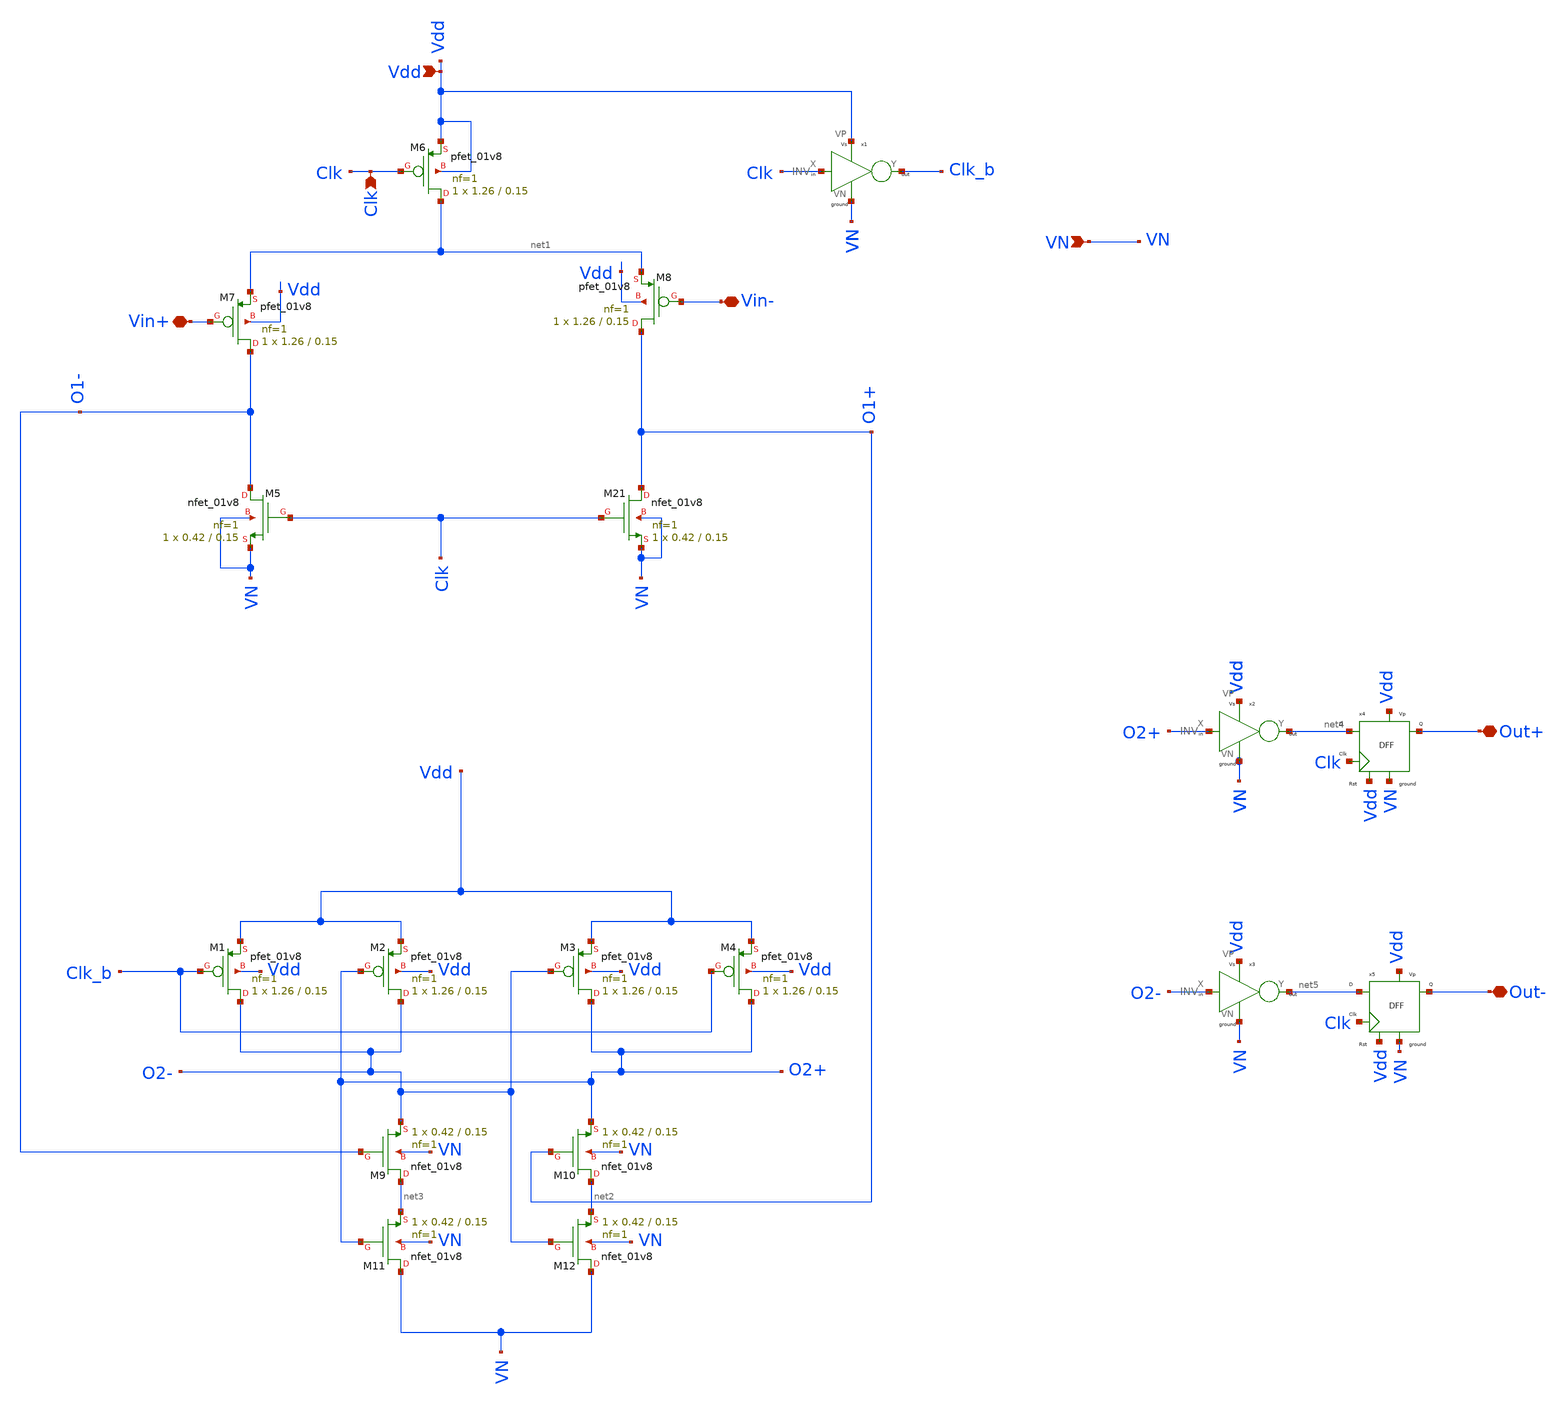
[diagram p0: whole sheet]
** sch_path: Blocks/Conv_comparator/Conv_comp.sch
**.subckt Conv_comp Vin+ Vin- Out+ Out- VN Vdd Clk
*.iopin Vin+
*.iopin Vin-
*.iopin Out+
*.iopin Out-
*.ipin VN
*.ipin Vdd
*.ipin Clk
XM6 net1 Clk Vdd Vdd sky130_fd_pr__pfet_01v8 L=0.15 W=1.26 nf=1 ad='int((nf+1)/2) * W/nf * 0.29' as='int((nf+2)/2) * W/nf * 0.29'
+ pd='2*int((nf+1)/2) * (W/nf + 0.29)' ps='2*int((nf+2)/2) * (W/nf + 0.29)' nrd='0.29 / W' nrs='0.29 / W'
+ sa=0 sb=0 sd=0 mult=1 m=1
XM7 O1- Vin+ net1 Vdd sky130_fd_pr__pfet_01v8 L=0.15 W=1.26 nf=1 ad='int((nf+1)/2) * W/nf * 0.29' as='int((nf+2)/2) * W/nf * 0.29'
+ pd='2*int((nf+1)/2) * (W/nf + 0.29)' ps='2*int((nf+2)/2) * (W/nf + 0.29)' nrd='0.29 / W' nrs='0.29 / W'
+ sa=0 sb=0 sd=0 mult=1 m=1
XM8 O1+ Vin- net1 Vdd sky130_fd_pr__pfet_01v8 L=0.15 W=1.26 nf=1 ad='int((nf+1)/2) * W/nf * 0.29' as='int((nf+2)/2) * W/nf * 0.29'
+ pd='2*int((nf+1)/2) * (W/nf + 0.29)' ps='2*int((nf+2)/2) * (W/nf + 0.29)' nrd='0.29 / W' nrs='0.29 / W'
+ sa=0 sb=0 sd=0 mult=1 m=1
XM5 O1- Clk VN VN sky130_fd_pr__nfet_01v8 L=0.15 W=0.42 nf=1 ad='int((nf+1)/2) * W/nf * 0.29' as='int((nf+2)/2) * W/nf * 0.29'
+ pd='2*int((nf+1)/2) * (W/nf + 0.29)' ps='2*int((nf+2)/2) * (W/nf + 0.29)' nrd='0.29 / W' nrs='0.29 / W'
+ sa=0 sb=0 sd=0 mult=1 m=1
XM21 O1+ Clk VN VN sky130_fd_pr__nfet_01v8 L=0.15 W=0.42 nf=1 ad='int((nf+1)/2) * W/nf * 0.29' as='int((nf+2)/2) * W/nf * 0.29'
+ pd='2*int((nf+1)/2) * (W/nf + 0.29)' ps='2*int((nf+2)/2) * (W/nf + 0.29)' nrd='0.29 / W' nrs='0.29 / W'
+ sa=0 sb=0 sd=0 mult=1 m=1
XM1 O2- Clk_b Vdd Vdd sky130_fd_pr__pfet_01v8 L=0.15 W=1.26 nf=1 ad='int((nf+1)/2) * W/nf * 0.29' as='int((nf+2)/2) * W/nf * 0.29'
+ pd='2*int((nf+1)/2) * (W/nf + 0.29)' ps='2*int((nf+2)/2) * (W/nf + 0.29)' nrd='0.29 / W' nrs='0.29 / W'
+ sa=0 sb=0 sd=0 mult=1 m=1
XM2 O2- O2+ Vdd Vdd sky130_fd_pr__pfet_01v8 L=0.15 W=1.26 nf=1 ad='int((nf+1)/2) * W/nf * 0.29' as='int((nf+2)/2) * W/nf * 0.29'
+ pd='2*int((nf+1)/2) * (W/nf + 0.29)' ps='2*int((nf+2)/2) * (W/nf + 0.29)' nrd='0.29 / W' nrs='0.29 / W'
+ sa=0 sb=0 sd=0 mult=1 m=1
XM3 O2+ O2- Vdd Vdd sky130_fd_pr__pfet_01v8 L=0.15 W=1.26 nf=1 ad='int((nf+1)/2) * W/nf * 0.29' as='int((nf+2)/2) * W/nf * 0.29'
+ pd='2*int((nf+1)/2) * (W/nf + 0.29)' ps='2*int((nf+2)/2) * (W/nf + 0.29)' nrd='0.29 / W' nrs='0.29 / W'
+ sa=0 sb=0 sd=0 mult=1 m=1
XM4 O2+ Clk_b Vdd Vdd sky130_fd_pr__pfet_01v8 L=0.15 W=1.26 nf=1 ad='int((nf+1)/2) * W/nf * 0.29' as='int((nf+2)/2) * W/nf * 0.29'
+ pd='2*int((nf+1)/2) * (W/nf + 0.29)' ps='2*int((nf+2)/2) * (W/nf + 0.29)' nrd='0.29 / W' nrs='0.29 / W'
+ sa=0 sb=0 sd=0 mult=1 m=1
XM9 net3 O1- O2- VN sky130_fd_pr__nfet_01v8 L=0.15 W=0.42 nf=1 ad='int((nf+1)/2) * W/nf * 0.29' as='int((nf+2)/2) * W/nf * 0.29'
+ pd='2*int((nf+1)/2) * (W/nf + 0.29)' ps='2*int((nf+2)/2) * (W/nf + 0.29)' nrd='0.29 / W' nrs='0.29 / W'
+ sa=0 sb=0 sd=0 mult=1 m=1
XM10 net2 O1+ O2+ VN sky130_fd_pr__nfet_01v8 L=0.15 W=0.42 nf=1 ad='int((nf+1)/2) * W/nf * 0.29' as='int((nf+2)/2) * W/nf * 0.29'
+ pd='2*int((nf+1)/2) * (W/nf + 0.29)' ps='2*int((nf+2)/2) * (W/nf + 0.29)' nrd='0.29 / W' nrs='0.29 / W'
+ sa=0 sb=0 sd=0 mult=1 m=1
XM11 VN O2+ net3 VN sky130_fd_pr__nfet_01v8 L=0.15 W=0.42 nf=1 ad='int((nf+1)/2) * W/nf * 0.29' as='int((nf+2)/2) * W/nf * 0.29'
+ pd='2*int((nf+1)/2) * (W/nf + 0.29)' ps='2*int((nf+2)/2) * (W/nf + 0.29)' nrd='0.29 / W' nrs='0.29 / W'
+ sa=0 sb=0 sd=0 mult=1 m=1
XM12 VN O2- net2 VN sky130_fd_pr__nfet_01v8 L=0.15 W=0.42 nf=1 ad='int((nf+1)/2) * W/nf * 0.29' as='int((nf+2)/2) * W/nf * 0.29'
+ pd='2*int((nf+1)/2) * (W/nf + 0.29)' ps='2*int((nf+2)/2) * (W/nf + 0.29)' nrd='0.29 / W' nrs='0.29 / W'
+ sa=0 sb=0 sd=0 mult=1 m=1
x1 Clk Clk_b Vdd VN INV
x2 O2+ net4 Vdd VN INV
x3 O2- net5 Vdd VN INV
x4 net4 Clk Vdd VN Vdd Out+ DFF
x5 net5 Clk Vdd VN Vdd Out- DFF
**.ends

* expanding   symbol:  pico_chipathon/component/INV/INV.sym # of pins=4
** sym_path: component/INV/INV.sym
** sch_path: component/INV/INV.sch
.subckt INV X Y VP VN
*.ipin X
*.opin Y
*.iopin VN
*.iopin VP
XM1 Y X VN VN sky130_fd_pr__nfet_01v8 L=0.15 W=0.42 nf=1 ad='int((nf+1)/2) * W/nf * 0.29' as='int((nf+2)/2) * W/nf * 0.29'
+ pd='2*int((nf+1)/2) * (W/nf + 0.29)' ps='2*int((nf+2)/2) * (W/nf + 0.29)' nrd='0.29 / W' nrs='0.29 / W'
+ sa=0 sb=0 sd=0 mult=1 m=1
XM2 Y X VP VP sky130_fd_pr__pfet_01v8 L=0.15 W=1.26 nf=1 ad='int((nf+1)/2) * W/nf * 0.29' as='int((nf+2)/2) * W/nf * 0.29'
+ pd='2*int((nf+1)/2) * (W/nf + 0.29)' ps='2*int((nf+2)/2) * (W/nf + 0.29)' nrd='0.29 / W' nrs='0.29 / W'
+ sa=0 sb=0 sd=0 mult=1 m=1
.ends


* expanding   symbol:  component/FlipFlops/DFF.sym # of pins=6
** sym_path: component/FlipFlops/DFF.sym
** sch_path: component/FlipFlops/DFF.sch
.subckt DFF D Clk RST VN VP Q
*.opin Q
*.iopin VN
*.iopin VP
*.ipin Clk
*.ipin D
*.ipin RST
x1 net2 net5 net4 VP VN NAND
x7 net4 Clk RST VP VN net2 NAND3
x3 Q net1 RST VP VN net3 NAND3
x4 net2 Clk net5 VP VN net1 NAND3
x5 net1 D RST VP VN net5 NAND3
x6 net3 net2 Q VP VN NAND
.ends


* expanding   symbol:  component/NAND2/NAND.sym # of pins=5
** sym_path: component/NAND2/NAND.sym
** sch_path: component/NAND2/NAND.sch
.subckt NAND B A Y VP VN
*.iopin VP
*.ipin A
*.ipin B
*.opin Y
*.iopin VN
XM1 Y A VP VP sky130_fd_pr__pfet_01v8 L=0.15 W=1.26 nf=1 ad='int((nf+1)/2) * W/nf * 0.29' as='int((nf+2)/2) * W/nf * 0.29'
+ pd='2*int((nf+1)/2) * (W/nf + 0.29)' ps='2*int((nf+2)/2) * (W/nf + 0.29)' nrd='0.29 / W' nrs='0.29 / W'
+ sa=0 sb=0 sd=0 mult=1 m=1
XM2 Y B VP VP sky130_fd_pr__pfet_01v8 L=0.15 W=1.26 nf=1 ad='int((nf+1)/2) * W/nf * 0.29' as='int((nf+2)/2) * W/nf * 0.29'
+ pd='2*int((nf+1)/2) * (W/nf + 0.29)' ps='2*int((nf+2)/2) * (W/nf + 0.29)' nrd='0.29 / W' nrs='0.29 / W'
+ sa=0 sb=0 sd=0 mult=1 m=1
XM3 Y A net1 net1 sky130_fd_pr__nfet_01v8 L=0.15 W=0.84 nf=1 ad='int((nf+1)/2) * W/nf * 0.29' as='int((nf+2)/2) * W/nf * 0.29'
+ pd='2*int((nf+1)/2) * (W/nf + 0.29)' ps='2*int((nf+2)/2) * (W/nf + 0.29)' nrd='0.29 / W' nrs='0.29 / W'
+ sa=0 sb=0 sd=0 mult=1 m=1
XM4 net1 B VN VN sky130_fd_pr__nfet_01v8 L=0.15 W=0.84 nf=1 ad='int((nf+1)/2) * W/nf * 0.29' as='int((nf+2)/2) * W/nf * 0.29'
+ pd='2*int((nf+1)/2) * (W/nf + 0.29)' ps='2*int((nf+2)/2) * (W/nf + 0.29)' nrd='0.29 / W' nrs='0.29 / W'
+ sa=0 sb=0 sd=0 mult=1 m=1
.ends


* expanding   symbol:  component/NAND3/NAND3.sym # of pins=6
** sym_path: component/NAND3/NAND3.sym
** sch_path: component/NAND3/NAND3.sch
.subckt NAND3 A B C VP VN Y
*.iopin VP
*.iopin VN
*.ipin A
*.ipin B
*.ipin C
*.opin Y
XM1 Y A net1 VN sky130_fd_pr__nfet_01v8 L=0.15 W=1.26 nf=1 ad='int((nf+1)/2) * W/nf * 0.29' as='int((nf+2)/2) * W/nf * 0.29'
+ pd='2*int((nf+1)/2) * (W/nf + 0.29)' ps='2*int((nf+2)/2) * (W/nf + 0.29)' nrd='0.29 / W' nrs='0.29 / W'
+ sa=0 sb=0 sd=0 mult=1 m=1
XM2 net1 B net2 VN sky130_fd_pr__nfet_01v8 L=0.15 W=1.26 nf=1 ad='int((nf+1)/2) * W/nf * 0.29' as='int((nf+2)/2) * W/nf * 0.29'
+ pd='2*int((nf+1)/2) * (W/nf + 0.29)' ps='2*int((nf+2)/2) * (W/nf + 0.29)' nrd='0.29 / W' nrs='0.29 / W'
+ sa=0 sb=0 sd=0 mult=1 m=1
XM3 net2 C VN VN sky130_fd_pr__nfet_01v8 L=0.15 W=1.26 nf=1 ad='int((nf+1)/2) * W/nf * 0.29' as='int((nf+2)/2) * W/nf * 0.29'
+ pd='2*int((nf+1)/2) * (W/nf + 0.29)' ps='2*int((nf+2)/2) * (W/nf + 0.29)' nrd='0.29 / W' nrs='0.29 / W'
+ sa=0 sb=0 sd=0 mult=1 m=1
XM4 Y A VP VP sky130_fd_pr__pfet_01v8 L=0.15 W=1.26 nf=1 ad='int((nf+1)/2) * W/nf * 0.29' as='int((nf+2)/2) * W/nf * 0.29'
+ pd='2*int((nf+1)/2) * (W/nf + 0.29)' ps='2*int((nf+2)/2) * (W/nf + 0.29)' nrd='0.29 / W' nrs='0.29 / W'
+ sa=0 sb=0 sd=0 mult=1 m=1
XM5 Y B VP VP sky130_fd_pr__pfet_01v8 L=0.15 W=1.26 nf=1 ad='int((nf+1)/2) * W/nf * 0.29' as='int((nf+2)/2) * W/nf * 0.29'
+ pd='2*int((nf+1)/2) * (W/nf + 0.29)' ps='2*int((nf+2)/2) * (W/nf + 0.29)' nrd='0.29 / W' nrs='0.29 / W'
+ sa=0 sb=0 sd=0 mult=1 m=1
XM6 Y C VP VP sky130_fd_pr__pfet_01v8 L=0.15 W=1.26 nf=1 ad='int((nf+1)/2) * W/nf * 0.29' as='int((nf+2)/2) * W/nf * 0.29'
+ pd='2*int((nf+1)/2) * (W/nf + 0.29)' ps='2*int((nf+2)/2) * (W/nf + 0.29)' nrd='0.29 / W' nrs='0.29 / W'
+ sa=0 sb=0 sd=0 mult=1 m=1
.ends

.end
